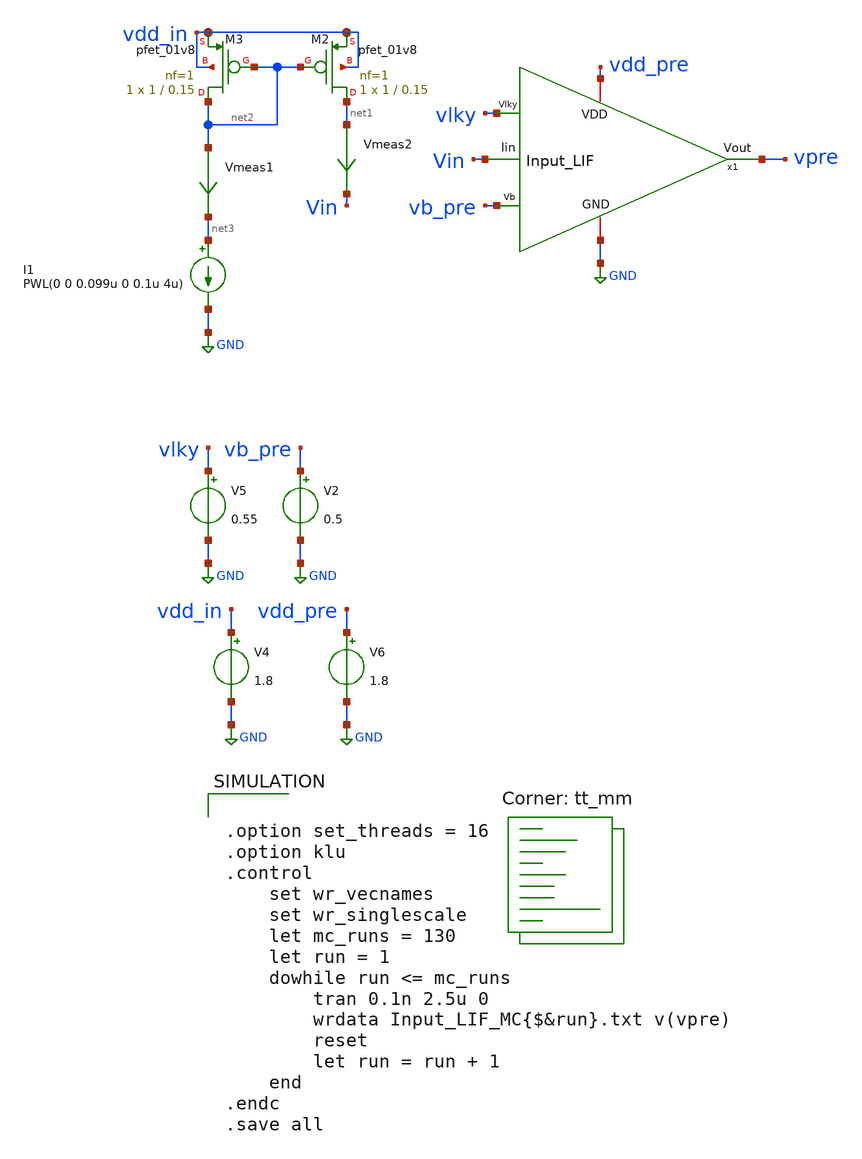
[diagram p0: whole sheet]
** sch_path: SNN/Input_LIF_MC_tb.sch
**.subckt Input_LIF_MC_tb
V2 vb_pre GND 0.5
I1 net3 GND PWL(0 0 0.099u 0 0.1u 4u)
XM2 net1 net2 vdd_in vdd_in sky130_fd_pr__pfet_01v8 L=0.15 W=1 nf=1 ad='int((nf+1)/2) * W/nf * 0.29'
+ as='int((nf+2)/2) * W/nf * 0.29' pd='2*int((nf+1)/2) * (W/nf + 0.29)' ps='2*int((nf+2)/2) * (W/nf + 0.29)'
+ nrd='0.29 / W' nrs='0.29 / W' sa=0 sb=0 sd=0 mult=1 m=1
XM3 net2 net2 vdd_in vdd_in sky130_fd_pr__pfet_01v8 L=0.15 W=1 nf=1 ad='int((nf+1)/2) * W/nf * 0.29'
+ as='int((nf+2)/2) * W/nf * 0.29' pd='2*int((nf+1)/2) * (W/nf + 0.29)' ps='2*int((nf+2)/2) * (W/nf + 0.29)'
+ nrd='0.29 / W' nrs='0.29 / W' sa=0 sb=0 sd=0 mult=1 m=1
Vmeas1 net2 net3 0
.save i(vmeas1)
Vmeas2 net1 Vin 0
.save i(vmeas2)
V4 vdd_in GND 1.8
V5 vlky GND 0.55
x1 vlky vb_pre vdd_pre vpre GND Vin Input_LIF
V6 vdd_pre GND 1.8
**** begin user architecture code


.option set_threads = 16
.option klu
.control
	set wr_vecnames
	set wr_singlescale
	let mc_runs = 130
	let run = 1
	dowhile run <= mc_runs
		tran 0.1n 2.5u 0
		wrdata Input_LIF_MC{$&run}.txt v(vpre)
		reset
		let run = run + 1
	end
.endc
.save all


.lib $::SKYWATER_MODELS/sky130.lib.spice tt_mm
**** end user architecture code
**.ends

* expanding   symbol:  /home/ricardo/RATT_repos/Proyectos_xschem/SNN/Input_LIF.sym # of pins=6
** sym_path: Final_Design/Input_LIF.sym
** sch_path: Final_Design/Input_LIF.sch
.subckt Input_LIF Vlky Vb VDD Vout GND Iin
*.iopin GND
*.ipin Vb
*.iopin VDD
*.opin Vout
*.ipin Iin
*.ipin Vlky
XM5 net3 Vb GND GND sky130_fd_pr__nfet_01v8 L=0.15 W=5 nf=1 ad='int((nf+1)/2) * W/nf * 0.29' as='int((nf+2)/2) * W/nf * 0.29'
+ pd='2*int((nf+1)/2) * (W/nf + 0.29)' ps='2*int((nf+2)/2) * (W/nf + 0.29)' nrd='0.29 / W' nrs='0.29 / W'
+ sa=0 sb=0 sd=0 mult=1 m=1
XM4 net1 net2 net3 GND sky130_fd_pr__nfet_01v8 L=0.15 W=1.5 nf=1 ad='int((nf+1)/2) * W/nf * 0.29' as='int((nf+2)/2) * W/nf * 0.29'
+ pd='2*int((nf+1)/2) * (W/nf + 0.29)' ps='2*int((nf+2)/2) * (W/nf + 0.29)' nrd='0.29 / W' nrs='0.29 / W'
+ sa=0 sb=0 sd=0 mult=1 m=1
XM3 net1 net2 VDD VDD sky130_fd_pr__pfet_01v8 L=20 W=1 nf=1 ad='int((nf+1)/2) * W/nf * 0.29' as='int((nf+2)/2) * W/nf * 0.29'
+ pd='2*int((nf+1)/2) * (W/nf + 0.29)' ps='2*int((nf+2)/2) * (W/nf + 0.29)' nrd='0.29 / W' nrs='0.29 / W'
+ sa=0 sb=0 sd=0 mult=1 m=1
XC2 net1 GND sky130_fd_pr__cap_mim_m3_1 W=10 L=5 MF=1 m=1
XM2 Iin net1 GND GND sky130_fd_pr__nfet_01v8 L=20 W=1 nf=1 ad='int((nf+1)/2) * W/nf * 0.29' as='int((nf+2)/2) * W/nf * 0.29'
+ pd='2*int((nf+1)/2) * (W/nf + 0.29)' ps='2*int((nf+2)/2) * (W/nf + 0.29)' nrd='0.29 / W' nrs='0.29 / W'
+ sa=0 sb=0 sd=0 mult=1 m=1
XC1 Iin GND sky130_fd_pr__cap_mim_m3_1 W=20 L=20 MF=1 m=1
XM10 net4 Vout GND GND sky130_fd_pr__nfet_01v8 L=0.15 W=1.5 nf=1 ad='int((nf+1)/2) * W/nf * 0.29' as='int((nf+2)/2) * W/nf * 0.29'
+ pd='2*int((nf+1)/2) * (W/nf + 0.29)' ps='2*int((nf+2)/2) * (W/nf + 0.29)' nrd='0.29 / W' nrs='0.29 / W'
+ sa=0 sb=0 sd=0 mult=1 m=1
XM7 net2 Iin net4 GND sky130_fd_pr__nfet_01v8 L=0.15 W=1.5 nf=1 ad='int((nf+1)/2) * W/nf * 0.29' as='int((nf+2)/2) * W/nf * 0.29'
+ pd='2*int((nf+1)/2) * (W/nf + 0.29)' ps='2*int((nf+2)/2) * (W/nf + 0.29)' nrd='0.29 / W' nrs='0.29 / W'
+ sa=0 sb=0 sd=0 mult=1 m=1
XM6 net2 Iin VDD VDD sky130_fd_pr__pfet_01v8 L=0.15 W=1.5 nf=1 ad='int((nf+1)/2) * W/nf * 0.29' as='int((nf+2)/2) * W/nf * 0.29'
+ pd='2*int((nf+1)/2) * (W/nf + 0.29)' ps='2*int((nf+2)/2) * (W/nf + 0.29)' nrd='0.29 / W' nrs='0.29 / W'
+ sa=0 sb=0 sd=0 mult=1 m=1
XM9 Vout net2 net4 GND sky130_fd_pr__nfet_01v8 L=0.15 W=1.5 nf=1 ad='int((nf+1)/2) * W/nf * 0.29' as='int((nf+2)/2) * W/nf * 0.29'
+ pd='2*int((nf+1)/2) * (W/nf + 0.29)' ps='2*int((nf+2)/2) * (W/nf + 0.29)' nrd='0.29 / W' nrs='0.29 / W'
+ sa=0 sb=0 sd=0 mult=1 m=1
XM8 Vout net2 VDD VDD sky130_fd_pr__pfet_01v8 L=0.15 W=5 nf=1 ad='int((nf+1)/2) * W/nf * 0.29' as='int((nf+2)/2) * W/nf * 0.29'
+ pd='2*int((nf+1)/2) * (W/nf + 0.29)' ps='2*int((nf+2)/2) * (W/nf + 0.29)' nrd='0.29 / W' nrs='0.29 / W'
+ sa=0 sb=0 sd=0 mult=1 m=1
XM1 Iin Vlky GND GND sky130_fd_pr__nfet_01v8 L=0.15 W=1.5 nf=1 ad='int((nf+1)/2) * W/nf * 0.29' as='int((nf+2)/2) * W/nf * 0.29'
+ pd='2*int((nf+1)/2) * (W/nf + 0.29)' ps='2*int((nf+2)/2) * (W/nf + 0.29)' nrd='0.29 / W' nrs='0.29 / W'
+ sa=0 sb=0 sd=0 mult=1 m=1
.ends

.GLOBAL GND
.end
